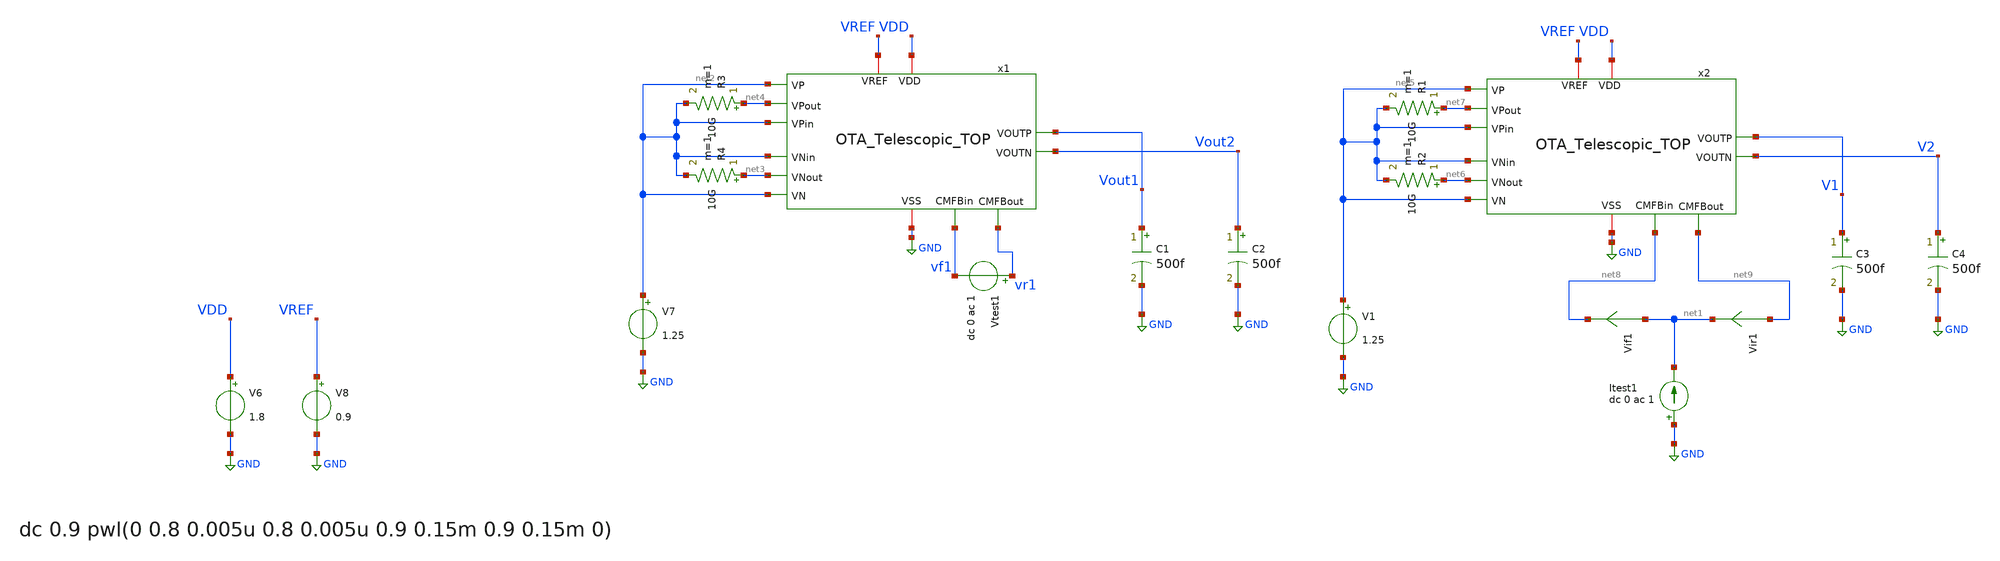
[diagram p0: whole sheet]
** sch_path: Differential_OTA_Telescopic_IHP/OTA_Telescopic_TOP_TB_CMFB.sch
**.subckt OTA_Telescopic_TOP_TB_CMFB
V7 net2 GND 1.25
C1 Vout1 GND 500f m=1
C2 Vout2 GND 500f m=1
x1 VDD GND net4 net2 net2 Vout2 Vout1 net2 net3 net2 VREF vf1 vr1 OTA_Telescopic_TOP
V6 VDD GND 1.8
V8 VREF GND 0.9
Vtest1 vr1 vf1 dc 0 ac 1
Vif1 net1 net8 0
.save i(vif1)
Vir1 net9 net1 0
.save i(vir1)
Itest1 GND net1 dc 0 ac 1
R3 net4 net2 10G m=1
R4 net3 net2 10G m=1
V1 net5 GND 1.25
C3 V1 GND 500f m=1
C4 V2 GND 500f m=1
x2 VDD GND net7 net5 net5 V2 V1 net5 net6 net5 VREF net8 net9 OTA_Telescopic_TOP
R1 net7 net5 10G m=1
R2 net6 net5 10G m=1
**** begin user architecture code

** opencircuitdesign pdks install
.lib cornerMOSlv.lib mos_tt
.lib cornerRES.lib res_typ
.temp 65



.op

.save all
*OTA
.save @m.x1.xm1.msky130_fd_pr__nfet_01v8_lvt[id]
.save @m.x1.xm1.msky130_fd_pr__nfet_01v8_lvt[gm]
.save @m.x1.xm2.msky130_fd_pr__nfet_01v8_lvt[id]
.save @m.x1.xm2.msky130_fd_pr__nfet_01v8_lvt[gm]

.save @m.x1.xm9.msky130_fd_pr__pfet_01v8_lvt[id]
.save @m.x1.xm9.msky130_fd_pr__pfet_01v8_lvt[gm]
.save @m.x1.xm10.msky130_fd_pr__pfet_01v8_lvt[id]
.save @m.x1.xm10.msky130_fd_pr__pfet_01v8_lvt[gm]

.save @m.x1.xm0.msky130_fd_pr__nfet_01v8_lvt[id]

.save @m.x1.xm1.msky130_fd_pr__nfet_01v8_lvt[vdssat]


.save @m.x1.xm13.msky130_fd_pr__nfet_01v8_lvt[id]
.save @m.x1.xm14.msky130_fd_pr__nfet_01v8_lvt[id]
.save @m.x1.xm15.msky130_fd_pr__pfet_01v8_lvt[id]
.save @m.x1.xm16.msky130_fd_pr__nfet_01v8_lvt[id]
.save @m.x1.xm17.msky130_fd_pr__nfet_01v8_lvt[id]

.save @m.x1.xm18.msky130_fd_pr__pfet_01v8_lvt[id]
.save @m.x1.xm19.msky130_fd_pr__nfet_01v8_lvt[id]

*CMFB
.save @m.x2.xm0.msky130_fd_pr__pfet_01v8_lvt[id]
.save @m.x2.xm1.msky130_fd_pr__pfet_01v8_lvt[id]
.save @m.x2.xm1.msky130_fd_pr__pfet_01v8_lvt[gm]
.save @m.x2.xm2.msky130_fd_pr__pfet_01v8_lvt[id]
.save @m.x2.xm2.msky130_fd_pr__pfet_01v8_lvt[gm]
.save @m.x2.xm3.msky130_fd_pr__pfet_01v8_lvt[id]
.save @m.x2.xm3.msky130_fd_pr__pfet_01v8_lvt[gm]
.save @m.x2.xm4.msky130_fd_pr__pfet_01v8_lvt[id]
.save @m.x2.xm4.msky130_fd_pr__pfet_01v8_lvt[gm]
.save @m.x2.xm5.msky130_fd_pr__pfet_01v8_lvt[id]
.save @m.x2.xm5.msky130_fd_pr__pfet_01v8_lvt[gm]
.save @m.x2.xm6.msky130_fd_pr__pfet_01v8_lvt[id]
.save @m.x2.xm6.msky130_fd_pr__pfet_01v8_lvt[gm]

.save @m.x2.xm7.msky130_fd_pr__nfet_01v8_lvt[id]
.save @m.x2.xm7.msky130_fd_pr__nfet_01v8_lvt[gm]
.save @m.x2.xm8.msky130_fd_pr__nfet_01v8_lvt[id]
.save @m.x2.xm8.msky130_fd_pr__nfet_01v8_lvt[gm]



.control

let vdssat_M1 = @m.x1.xm1.msky130_fd_pr__nfet_01v8_lvt[vdsat]
let vdssat_M3 = @m.x1.xm3.msky130_fd_pr__nfet_01v8_lvt[vdsat]
let vdssat_M5 = @m.x1.xm5.msky130_fd_pr__pfet_01v8_lvt[vdsat]
let vdssat_M7 = @m.x1.xm7.msky130_fd_pr__pfet_01v8_lvt[vdsat]
let vdssat_M0 = @m.x1.xm0.msky130_fd_pr__nfet_01v8_lvt[vdsat]

let vdssat_M9 = @m.x1.xm9.msky130_fd_pr__pfet_01v8_lvt[vdsat]
let vdssat_M11 = @m.x1.xm11.msky130_fd_pr__nfet_01v8_lvt[vdsat]

print vdssat_M1
print vdssat_M3
print vdssat_M5
print vdssat_M7
print vdssat_M0
print vdssat_M9
print vdssat_M11

let ro_M1 = 1/@m.x1.xm1.msky130_fd_pr__nfet_01v8_lvt[gds]
let ro_M3 = 1/@m.x1.xm3.msky130_fd_pr__nfet_01v8_lvt[gds]
let ro_M5 = 1/@m.x1.xm5.msky130_fd_pr__pfet_01v8_lvt[gds]
let ro_M7 = 1/@m.x1.xm7.msky130_fd_pr__pfet_01v8_lvt[gds]
let ro_M0 = 1/@m.x1.xm0.msky130_fd_pr__nfet_01v8_lvt[gds]

print ro_M1
print ro_M3
print ro_M5
print ro_M7
print ro_M0

let gm_M1 = @m.x1.xm1.msky130_fd_pr__nfet_01v8_lvt[gm]
let gm_M3 = @m.x1.xm3.msky130_fd_pr__nfet_01v8_lvt[gm]
let gm_M5 = @m.x1.xm5.msky130_fd_pr__pfet_01v8_lvt[gm]
let gm_M7 = @m.x1.xm7.msky130_fd_pr__pfet_01v8_lvt[gm]
let gm_M0 = @m.x1.xm0.msky130_fd_pr__nfet_01v8_lvt[gm]

print gm_M1
print gm_M3
print gm_M5
print gm_M7
print gm_M0

let gmb_M3 = @m.x1.xm3.msky130_fd_pr__nfet_01v8_lvt[gmbs]
let gmb_M5 = @m.x1.xm5.msky130_fd_pr__pfet_01v8_lvt[gmbs]

print gmb_M3
print gmb_M5


let cgg_M0 = @m.x1.xm0.msky130_fd_pr__nfet_01v8_lvt[cgg]
print cgg_M0


*CMFB

let x2_vdssat_M0 = @m.x2.xm0.msky130_fd_pr__pfet_01v8_lvt[vdsat]
let x2_vth_M0 = @m.x2.xm0.msky130_fd_pr__pfet_01v8_lvt[vth]

print x2_vdssat_M0
print x2_vth_M0

.endc






.options savecurrents reltol=1e-3 abstol=1e-12 gmin=1e-15
.control
save all

* Operating Point Analysis
op
remzerovec
let cgg_M0 = @m.x1.xm0.msky130_fd_pr__nfet_01v8_lvt[cgg]
print cgg_M0
write OTA_Telescopic_TB2_STB.raw
set appendwrite

* AC Analysis
ac dec 10 1 5G
remzerovec
write Middlebrook.raw
set appendwrite

* Middlebrook's Method
let tv=-v(vr1)/v(vf1)
let ti=-i(vir1)/i(vif1)
let tmb=(tv*ti - 1)/(tv + ti + 2)

let Av = db(tmb)
meas ac Ao MAX Av
let ABW = Ao-3
meas ac BW WHEN Av=ABW
meas ac UGBW WHEN Av=0

* Phase margin (PM)
let phase_vec= 180/pi*cph(tmb)
meas ac phase FIND phase_vec WHEN frequency=UGBW
let PM = phase+180
print PM

* Gain margin (GM)
meas ac freq180 FIND frequency WHEN phase_vec=-180
meas ac gain FIND Av WHEN frequency=freq180
let GM = 0-gain
print GM

plot Av ylabel 'Magnitude - Middlebrook'
plot phase_vec ylabel 'Phase - Middlebrook'

write Middlebrook_.raw

wrdata STB_Av_ Av
wrdata STB_ph_ phase_vec

*quit

.endc


**** end user architecture code
**.ends
.GLOBAL GND
.end
